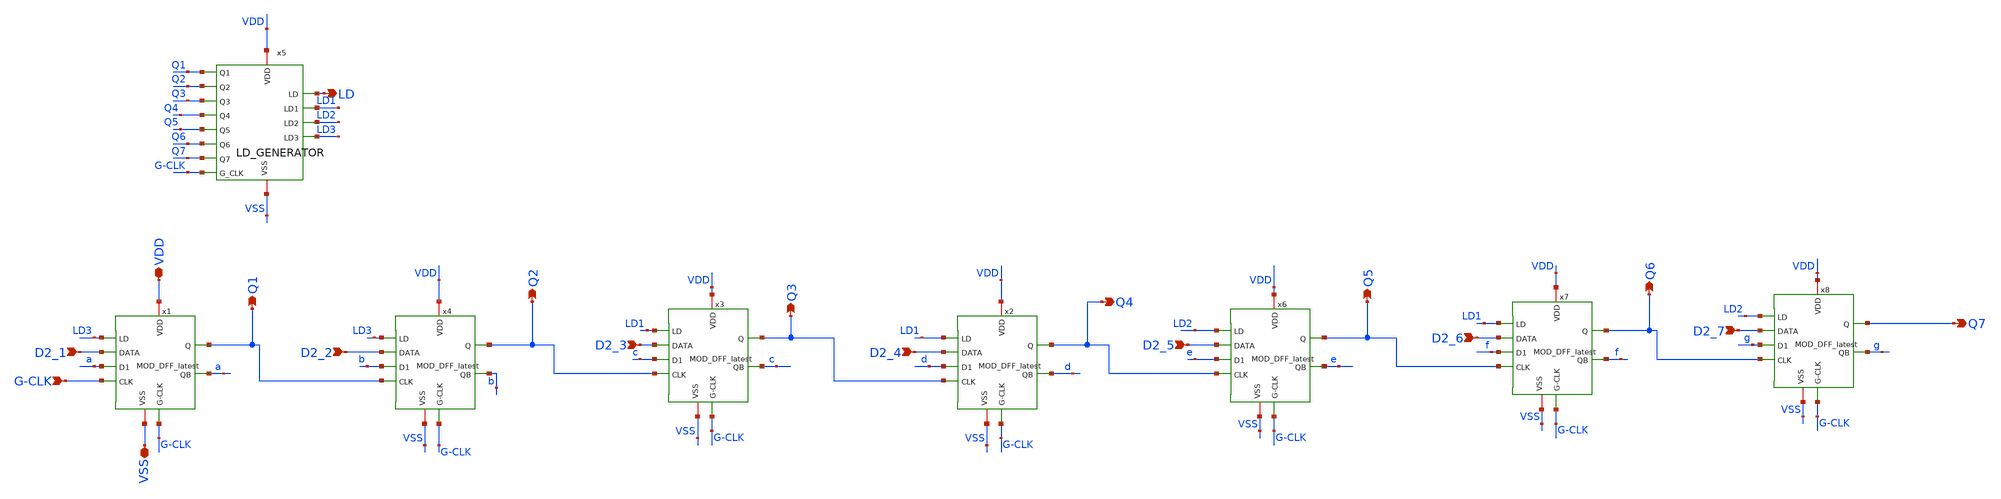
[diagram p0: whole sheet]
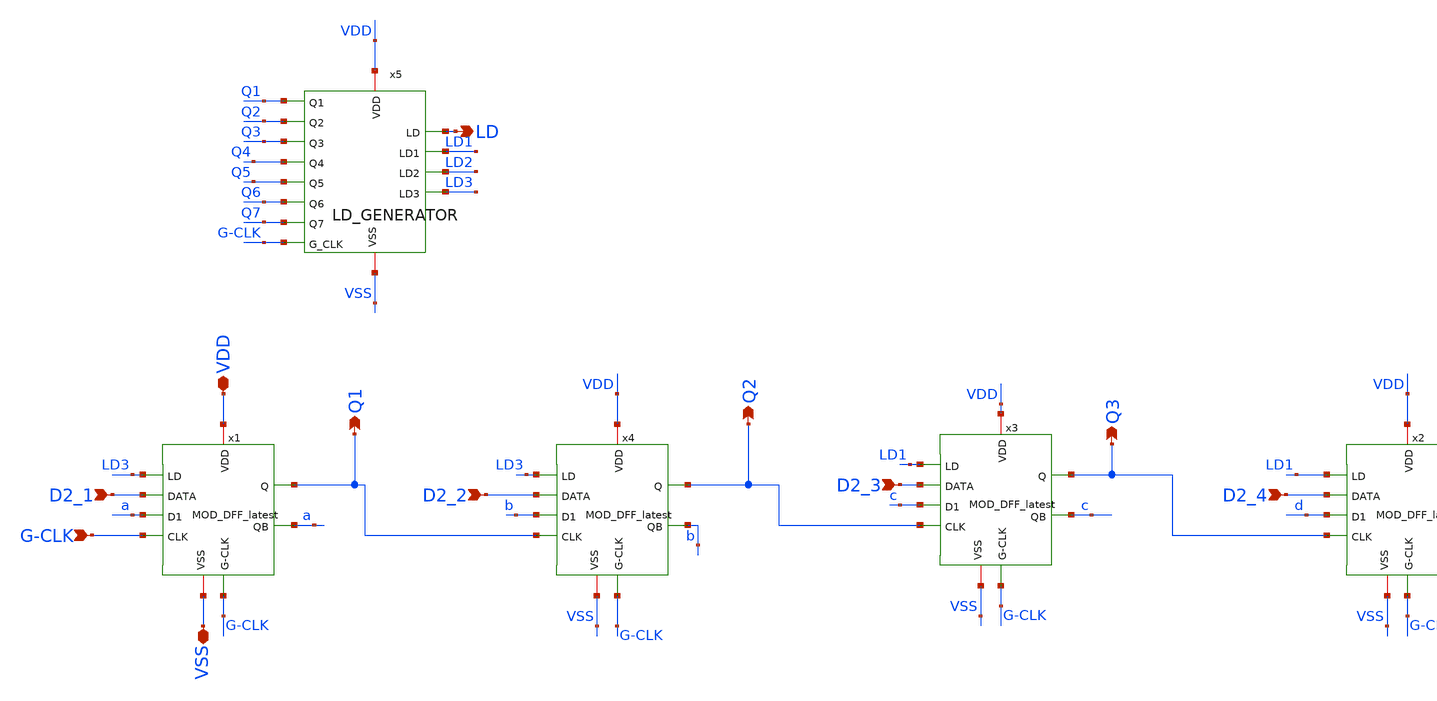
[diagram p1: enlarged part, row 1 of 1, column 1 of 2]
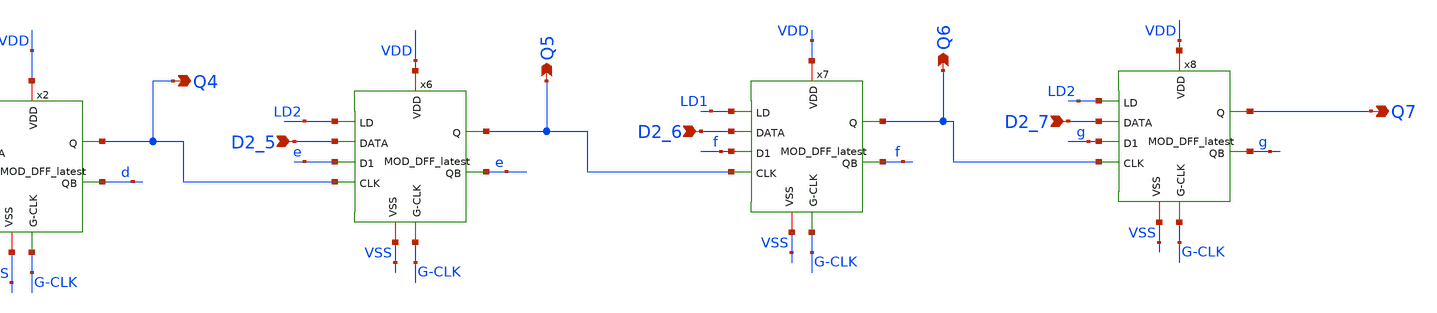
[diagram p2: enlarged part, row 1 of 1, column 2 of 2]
** sch_path: Xschem/PLL_TOP_Schematics/7b_counter_new.sch
**.subckt 7b_counter_new VDD VSS Q3 Q1 D2_1 D2_2 D2_3 G-CLK Q2 LD D2_4 Q4 D2_5 Q5 Q6 D2_6 Q7 D2_7
*.iopin VDD
*.iopin VSS
*.opin Q3
*.opin Q1
*.ipin D2_1
*.ipin D2_2
*.ipin D2_3
*.ipin G-CLK
*.opin Q2
*.opin LD
*.ipin D2_4
*.opin Q4
*.ipin D2_5
*.opin Q5
*.opin Q6
*.ipin D2_6
*.opin Q7
*.ipin D2_7
x1 VDD LD3 D2_1 Q1 a a VSS G-CLK G-CLK MOD_DFF_latest
x3 VDD LD1 D2_3 Q3 c c VSS Q2 G-CLK MOD_DFF_latest
x4 VDD LD3 D2_2 Q2 b b VSS Q1 G-CLK MOD_DFF_latest
x2 VDD LD1 D2_4 Q4 d d VSS Q3 G-CLK MOD_DFF_latest
x6 VDD LD2 D2_5 Q5 e e VSS Q4 G-CLK MOD_DFF_latest
x7 VDD LD1 D2_6 Q6 f f VSS Q5 G-CLK MOD_DFF_latest
x8 VDD LD2 D2_7 Q7 g g VSS Q6 G-CLK MOD_DFF_latest
x5 Q1 VDD LD1 VSS LD2 Q2 LD3 Q3 Q4 Q5 LD Q6 Q7 G-CLK LD_GENERATOR
**.ends
.end
